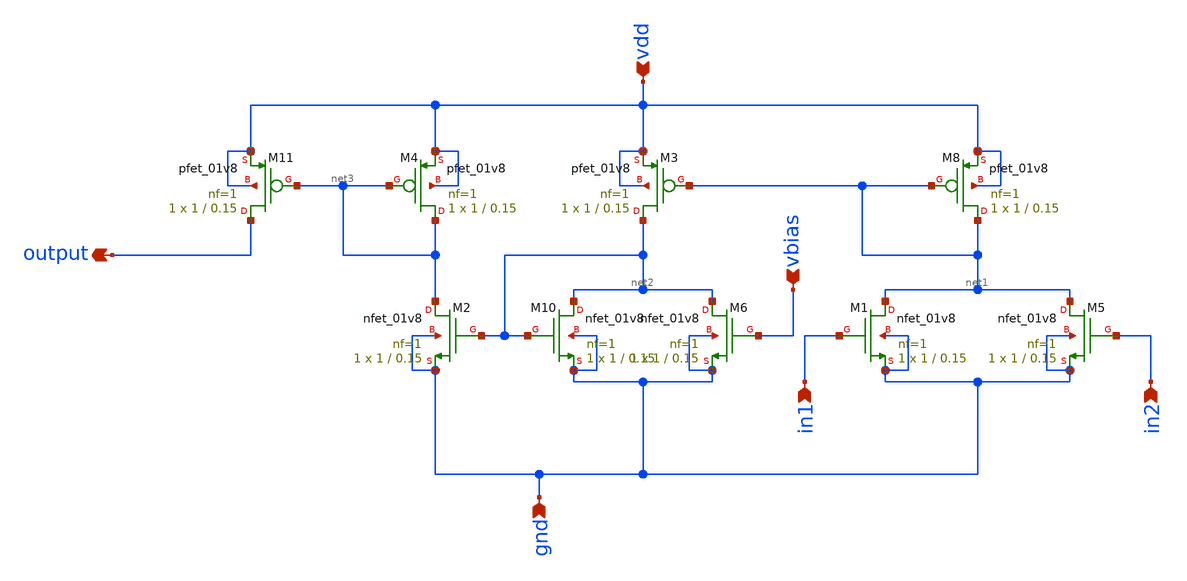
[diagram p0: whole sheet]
** sch_path: xschem/balaced-pd.sch
**.subckt balaced-pd vdd gnd output in1 in2 vbias
*.ipin vdd
*.ipin gnd
*.opin output
*.ipin in1
*.ipin in2
*.ipin vbias
XM10 net2 net2 gnd gnd sky130_fd_pr__nfet_01v8 L=0.15 W=1 nf=1 ad='int((nf+1)/2) * W/nf * 0.29' as='int((nf+2)/2) * W/nf * 0.29'
+ pd='2*int((nf+1)/2) * (W/nf + 0.29)' ps='2*int((nf+2)/2) * (W/nf + 0.29)' nrd='0.29 / W' nrs='0.29 / W'
+ sa=0 sb=0 sd=0 mult=1 m=1
XM11 output net3 vdd vdd sky130_fd_pr__pfet_01v8 L=0.15 W=1 nf=1 ad='int((nf+1)/2) * W/nf * 0.29' as='int((nf+2)/2) * W/nf * 0.29'
+ pd='2*int((nf+1)/2) * (W/nf + 0.29)' ps='2*int((nf+2)/2) * (W/nf + 0.29)' nrd='0.29 / W' nrs='0.29 / W'
+ sa=0 sb=0 sd=0 mult=1 m=1
XM3 net2 net1 vdd vdd sky130_fd_pr__pfet_01v8 L=0.15 W=1 nf=1 ad='int((nf+1)/2) * W/nf * 0.29' as='int((nf+2)/2) * W/nf * 0.29'
+ pd='2*int((nf+1)/2) * (W/nf + 0.29)' ps='2*int((nf+2)/2) * (W/nf + 0.29)' nrd='0.29 / W' nrs='0.29 / W'
+ sa=0 sb=0 sd=0 mult=1 m=1
XM4 net3 net3 vdd vdd sky130_fd_pr__pfet_01v8 L=0.15 W=1 nf=1 ad='int((nf+1)/2) * W/nf * 0.29' as='int((nf+2)/2) * W/nf * 0.29'
+ pd='2*int((nf+1)/2) * (W/nf + 0.29)' ps='2*int((nf+2)/2) * (W/nf + 0.29)' nrd='0.29 / W' nrs='0.29 / W'
+ sa=0 sb=0 sd=0 mult=1 m=1
XM8 net1 net1 vdd vdd sky130_fd_pr__pfet_01v8 L=0.15 W=1 nf=1 ad='int((nf+1)/2) * W/nf * 0.29' as='int((nf+2)/2) * W/nf * 0.29'
+ pd='2*int((nf+1)/2) * (W/nf + 0.29)' ps='2*int((nf+2)/2) * (W/nf + 0.29)' nrd='0.29 / W' nrs='0.29 / W'
+ sa=0 sb=0 sd=0 mult=1 m=1
XM1 net1 in1 gnd gnd sky130_fd_pr__nfet_01v8 L=0.15 W=1 nf=1 ad='int((nf+1)/2) * W/nf * 0.29' as='int((nf+2)/2) * W/nf * 0.29'
+ pd='2*int((nf+1)/2) * (W/nf + 0.29)' ps='2*int((nf+2)/2) * (W/nf + 0.29)' nrd='0.29 / W' nrs='0.29 / W'
+ sa=0 sb=0 sd=0 mult=1 m=1
XM2 net3 net2 gnd gnd sky130_fd_pr__nfet_01v8 L=0.15 W=1 nf=1 ad='int((nf+1)/2) * W/nf * 0.29' as='int((nf+2)/2) * W/nf * 0.29'
+ pd='2*int((nf+1)/2) * (W/nf + 0.29)' ps='2*int((nf+2)/2) * (W/nf + 0.29)' nrd='0.29 / W' nrs='0.29 / W'
+ sa=0 sb=0 sd=0 mult=1 m=1
XM5 net1 in2 gnd gnd sky130_fd_pr__nfet_01v8 L=0.15 W=1 nf=1 ad='int((nf+1)/2) * W/nf * 0.29' as='int((nf+2)/2) * W/nf * 0.29'
+ pd='2*int((nf+1)/2) * (W/nf + 0.29)' ps='2*int((nf+2)/2) * (W/nf + 0.29)' nrd='0.29 / W' nrs='0.29 / W'
+ sa=0 sb=0 sd=0 mult=1 m=1
XM6 net2 vbias gnd gnd sky130_fd_pr__nfet_01v8 L=0.15 W=1 nf=1 ad='int((nf+1)/2) * W/nf * 0.29' as='int((nf+2)/2) * W/nf * 0.29'
+ pd='2*int((nf+1)/2) * (W/nf + 0.29)' ps='2*int((nf+2)/2) * (W/nf + 0.29)' nrd='0.29 / W' nrs='0.29 / W'
+ sa=0 sb=0 sd=0 mult=1 m=1
**** begin user architecture code
 ** manual skywater pdks install (with patches applied)
* .lib $::SKYWATER_MODELS/models/sky130.lib.spice tt

** opencircuitdesign pdks install
.lib $::SKYWATER_MODELS/sky130.lib.spice tt

.param mc_mm_switch=0
.param mc_pr_switch=0



.tran 0.0005s 0.5s


**** end user architecture code
**.ends
.end
